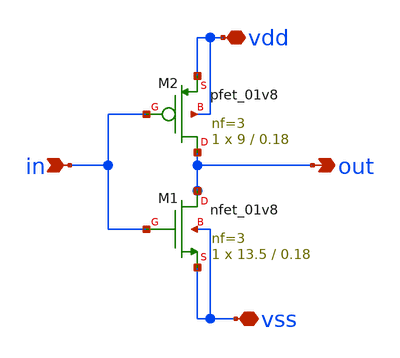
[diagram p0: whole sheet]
** sch_path: Day1/inverter/xschem/inverter.sch
**.subckt inverter in vdd vss out
*.ipin in
*.iopin vdd
*.iopin vss
*.opin out
XM1 out in vss vss sky130_fd_pr__nfet_01v8 L=0.18 W=13.5 nf=3 ad='int((nf+1)/2) * W/nf * 0.29' as='int((nf+2)/2) * W/nf * 0.29'
+ pd='2*int((nf+1)/2) * (W/nf + 0.29)' ps='2*int((nf+2)/2) * (W/nf + 0.29)' nrd='0.29 / W' nrs='0.29 / W'
+ sa=0 sb=0 sd=0 mult=1 m=1
XM2 out in vdd vdd sky130_fd_pr__pfet_01v8 L=0.18 W=9 nf=3 ad='int((nf+1)/2) * W/nf * 0.29' as='int((nf+2)/2) * W/nf * 0.29'
+ pd='2*int((nf+1)/2) * (W/nf + 0.29)' ps='2*int((nf+2)/2) * (W/nf + 0.29)' nrd='0.29 / W' nrs='0.29 / W'
+ sa=0 sb=0 sd=0 mult=1 m=1
**.ends
.end
